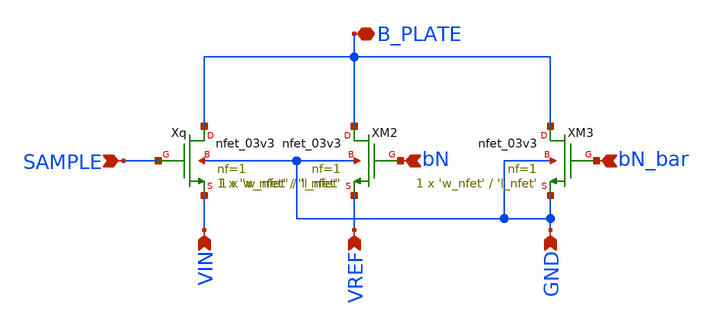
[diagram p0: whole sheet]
** sch_path: designs/libs/unit_switch.sch
**.subckt unit_switch GND VREF VIN SAMPLE B_PLATE bN bN_bar
*.ipin GND
*.ipin VREF
*.ipin VIN
*.ipin SAMPLE
*.iopin B_PLATE
*.ipin bN
*.ipin bN_bar
Xq B_PLATE SAMPLE VIN GND nfet_03v3 L='l_nfet' W='w_nfet' nf=1 ad='int((nf+1)/2) * W/nf * 0.18u' as='int((nf+2)/2) * W/nf * 0.18u'
+ pd='2*int((nf+1)/2) * (W/nf + 0.18u)' ps='2*int((nf+2)/2) * (W/nf + 0.18u)' nrd='0.18u / W' nrs='0.18u / W'
+ sa=0 sb=0 sd=0 m=1
XM2 B_PLATE bN VREF GND nfet_03v3 L='l_nfet' W='w_nfet' nf=1 ad='int((nf+1)/2) * W/nf * 0.18u' as='int((nf+2)/2) * W/nf * 0.18u'
+ pd='2*int((nf+1)/2) * (W/nf + 0.18u)' ps='2*int((nf+2)/2) * (W/nf + 0.18u)' nrd='0.18u / W' nrs='0.18u / W'
+ sa=0 sb=0 sd=0 m=1
XM3 B_PLATE bN_bar GND GND nfet_03v3 L='l_nfet' W='w_nfet' nf=1 ad='int((nf+1)/2) * W/nf * 0.18u' as='int((nf+2)/2) * W/nf * 0.18u'
+ pd='2*int((nf+1)/2) * (W/nf + 0.18u)' ps='2*int((nf+2)/2) * (W/nf + 0.18u)' nrd='0.18u / W' nrs='0.18u / W'
+ sa=0 sb=0 sd=0 m=1
**.ends
.end
